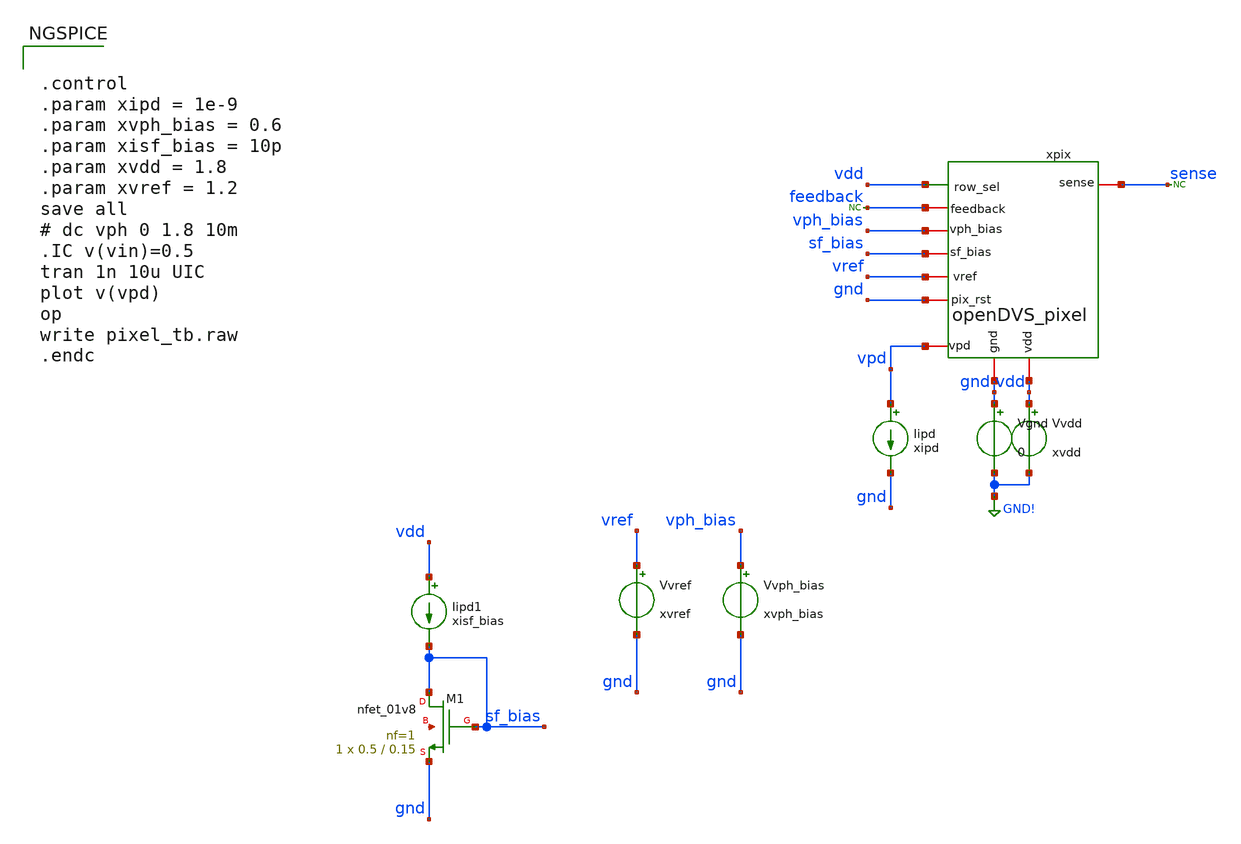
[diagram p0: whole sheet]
** sch_path: analog/xschem/pixel_tb.sch
**.subckt pixel_tb
xpix feedback gnd sense vdd vdd sf_bias gnd vref vpd vph_bias openDVS_pixel
Vgnd gnd GND! 0
Vvdd vdd GND! xvdd
Iipd vpd gnd xipd
XM1 sf_bias sf_bias gnd net1 sky130_fd_pr__nfet_01v8 L=0.15 W=0.5 nf=1 ad='int((1 + 1)/2) * 0.5 / 1 * 0.29'
+ as='int((1 + 2)/2) * 0.5 / 1 * 0.29' pd='2*int((1 + 1)/2) * (0.5 / 1 + 0.29)' ps='2*int((1 + 2)/2) * (0.5 / 1 + 0.29)'
+ nrd='0.29 / 0.5 ' nrs='0.29 / 0.5 ' sa=0 sb=0 sd=0 mult=1 m=1
Iipd1 vdd sf_bias xisf_bias
Vvref vref gnd xvref
Vvph_bias vph_bias gnd xvph_bias
* noconn sense
* noconn feedback
**** begin user architecture code

** opencircuitdesign pdks install
.lib $::SKYWATER_MODELS/sky130.lib.spice tt



.control
.param xipd = 1e-9
.param xvph_bias = 0.6
.param xisf_bias = 10p
.param xvdd = 1.8
.param xvref = 1.2
save all
# dc vph 0 1.8 10m
.IC v(vin)=0.5
tran 1n 10u UIC
plot v(vpd)
op
write pixel_tb.raw
.endc


**** end user architecture code
**.ends
.GLOBAL GND!
.end
